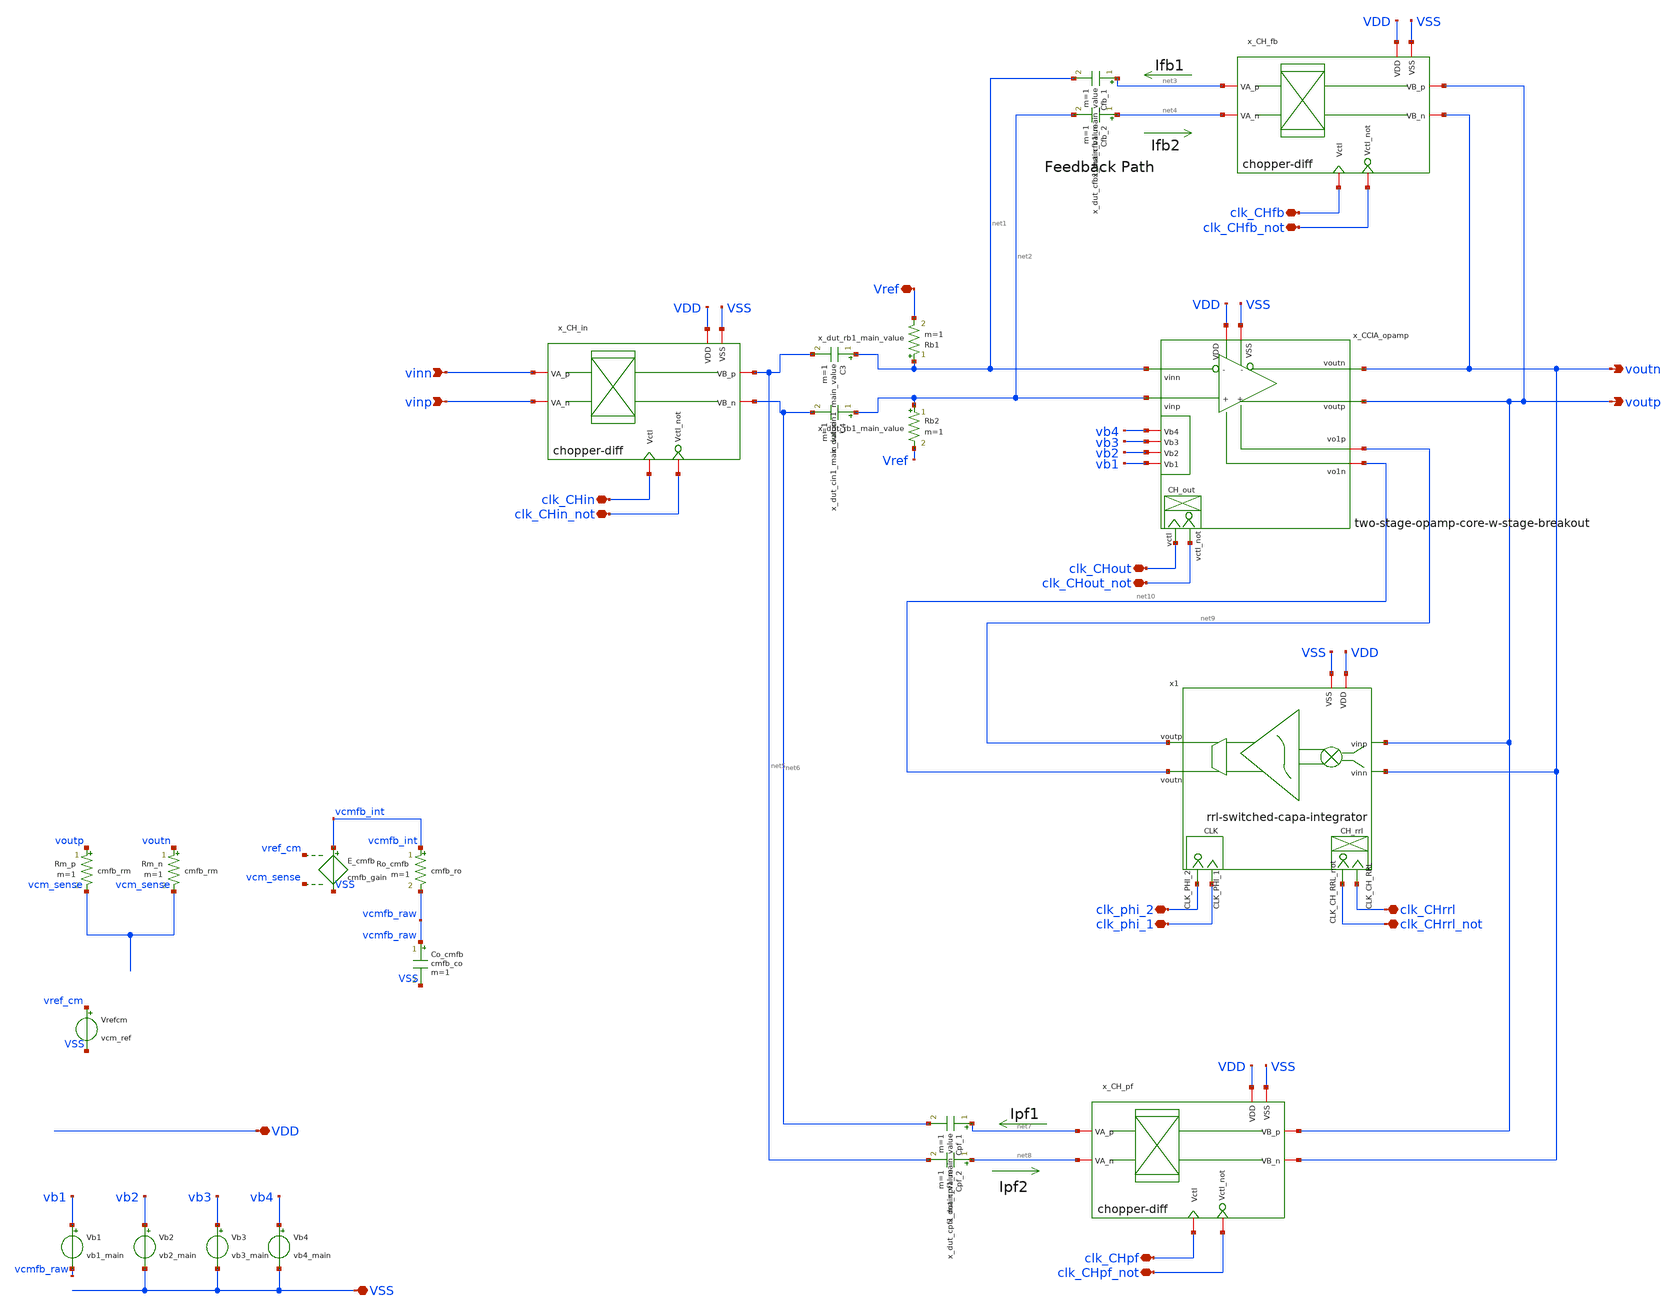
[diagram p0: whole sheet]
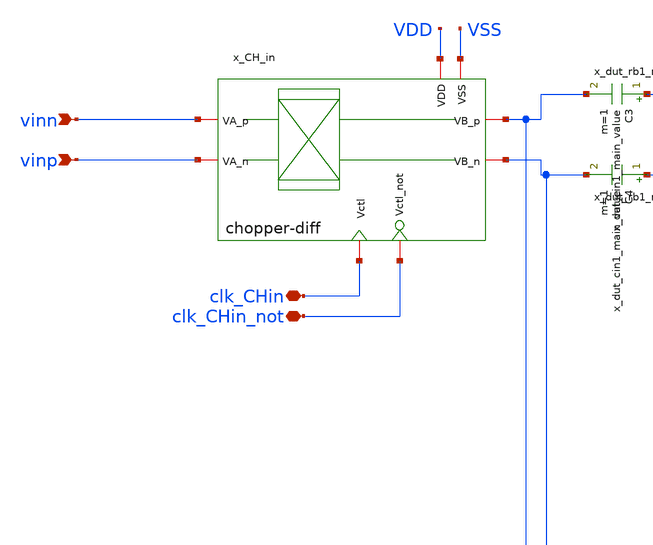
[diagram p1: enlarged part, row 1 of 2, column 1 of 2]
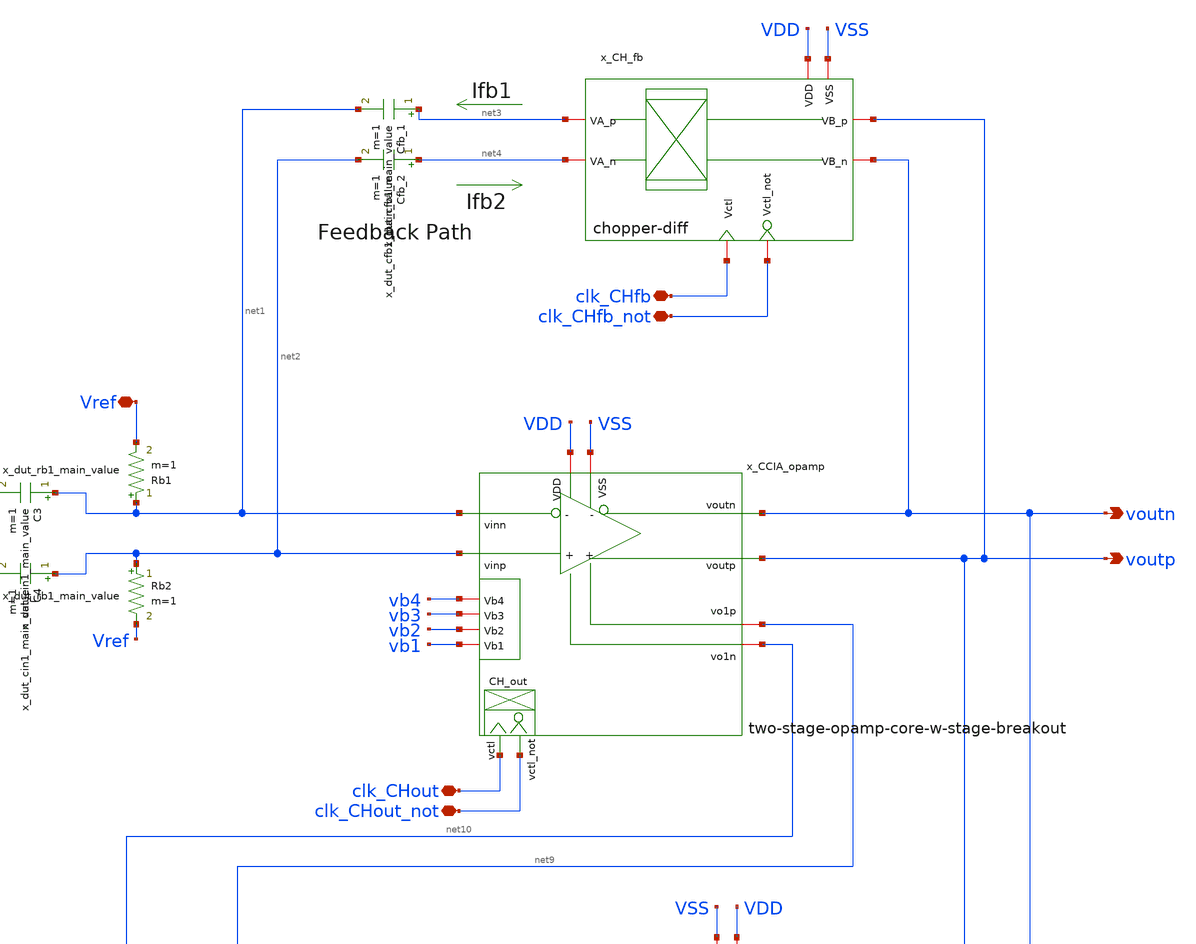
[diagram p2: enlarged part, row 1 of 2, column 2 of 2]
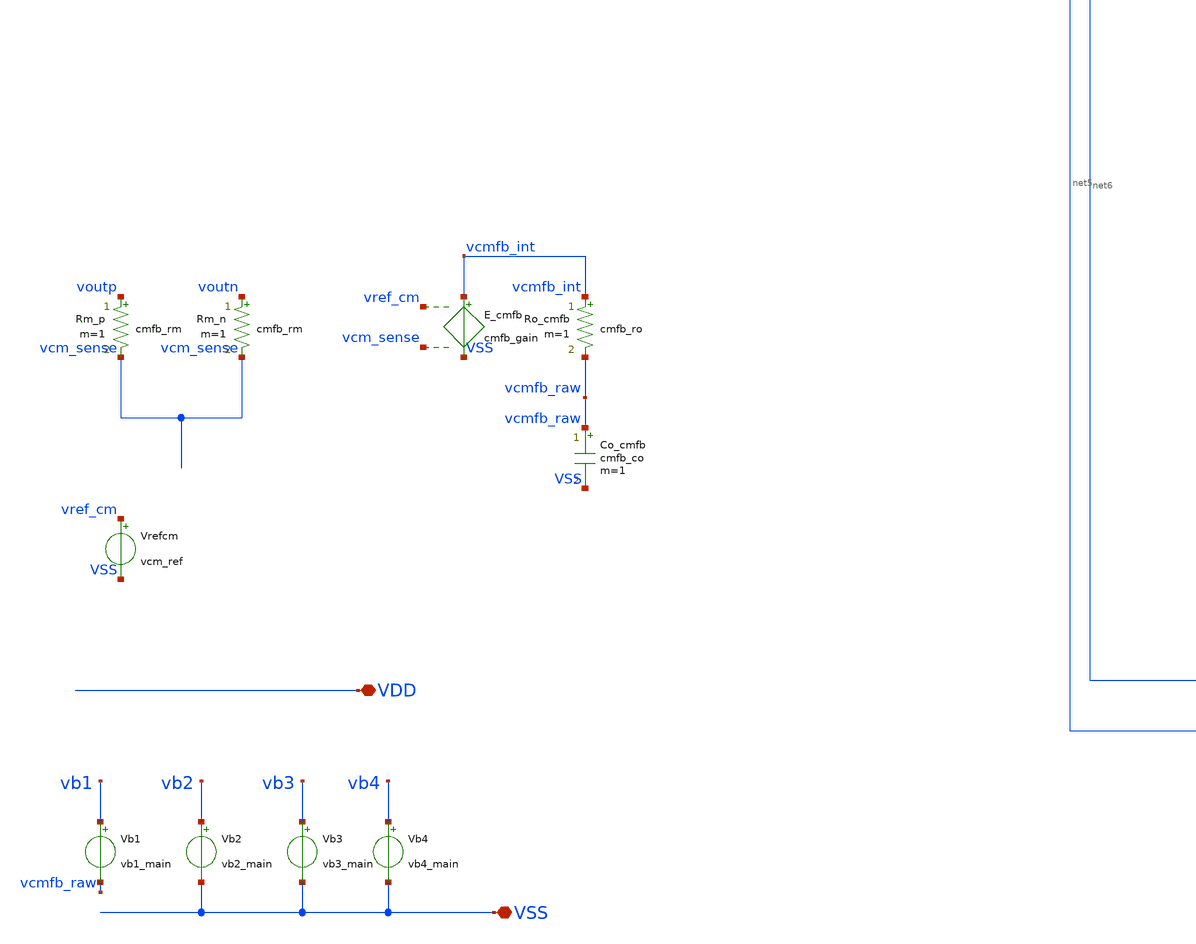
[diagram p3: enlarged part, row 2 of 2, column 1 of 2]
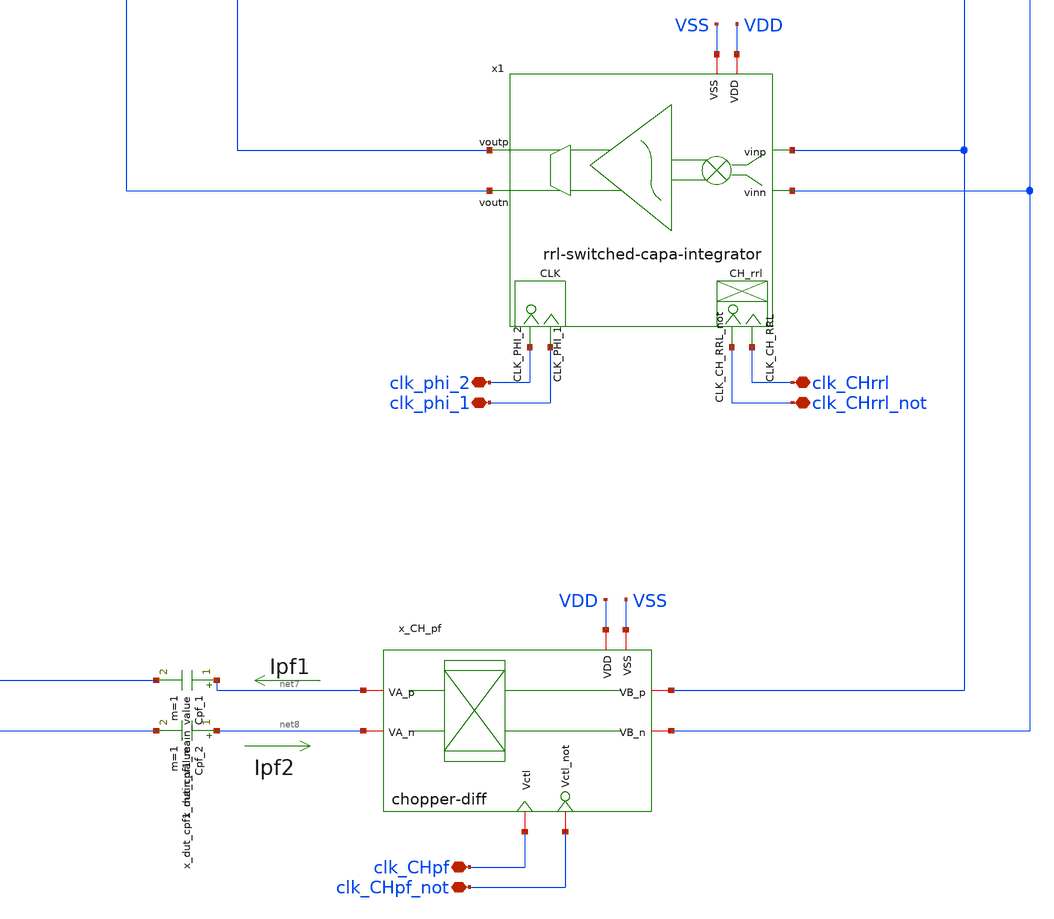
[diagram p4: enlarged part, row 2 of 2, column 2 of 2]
** sch_path: analog-db/drawings/ccia-02-QinwenFan-chopper-ripple-reduction/ccia-dut-chopper-w-positive-feedback-rrl-cmfb.sch
* Copyright 2026 MacAnalog Research Group
**.subckt ccia-dut-chopper-w-positive-feedback-rrl-cmfb VSS VDD voutn voutp clk_CHout clk_CHout_not
*+ clk_CHfb clk_CHfb_not clk_CHin clk_CHin_not vinn vinp Vref clk_CHpf clk_CHpf_not clk_CHrrl clk_CHrrl_not
*+ clk_phi_2 clk_phi_1
*.iopin VSS
*.iopin VDD
*.opin voutn
*.opin voutp
*.iopin clk_CHout
*.iopin clk_CHout_not
*.iopin clk_CHfb
*.iopin clk_CHfb_not
*.iopin clk_CHin
*.iopin clk_CHin_not
*.ipin vinn
*.ipin vinp
*.iopin Vref
*.iopin clk_CHpf
*.iopin clk_CHpf_not
*.iopin clk_CHrrl
*.iopin clk_CHrrl_not
*.iopin clk_phi_2
*.iopin clk_phi_1
Rm_p voutp vcm_sense cmfb_rm m=1
Rm_n voutn vcm_sense cmfb_rm m=1
E_cmfb vcmfb_int VSS vref_cm vcm_sense cmfb_gain
Ro_cmfb vcmfb_int vcmfb_raw cmfb_ro m=1
Co_cmfb vcmfb_raw VSS cmfb_co m=1
Vrefcm vref_cm VSS vcm_ref
x_CCIA_opamp VDD vb4 net1 voutn vb3 net2 vb2 voutp clk_CHout clk_CHout_not vb1 VSS net9 net10
+ two-stage-opamp-core-w-stage-breakout
Vb1 vb1 vcmfb_raw vb1_main
Vb2 vb2 VSS vb2_main
Vb3 vb3 VSS vb3_main
x_CH_fb clk_CHfb VDD voutp net3 clk_CHfb_not VSS voutn net4 chopper-diff
Cfb_1 net3 net1 x_dut_cfb1_main_value m=1
Cfb_2 net4 net2 x_dut_cfb1_main_value m=1
C3 net1 net5 x_dut_cin1_main_value m=1
C4 net2 net6 x_dut_cin1_main_value m=1
x_CH_in clk_CHin VDD net5 vinn clk_CHin_not VSS net6 vinp chopper-diff
Rb1 net1 Vref x_dut_rb1_main_value m=1
Rb2 net2 Vref x_dut_rb1_main_value m=1
Vb4 vb4 VSS vb4_main
x_CH_pf clk_CHpf VDD voutp net7 clk_CHpf_not VSS voutn net8 chopper-diff
Cpf_1 net7 net6 x_dut_cpf1_main_value m=1
Cpf_2 net8 net5 x_dut_cpf1_main_value m=1
x1 voutp voutn clk_phi_1 clk_phi_2 clk_CHrrl clk_CHrrl_not net10 net9 VDD VSS
+ rrl-switched-capa-integrator
**.ends
.end
